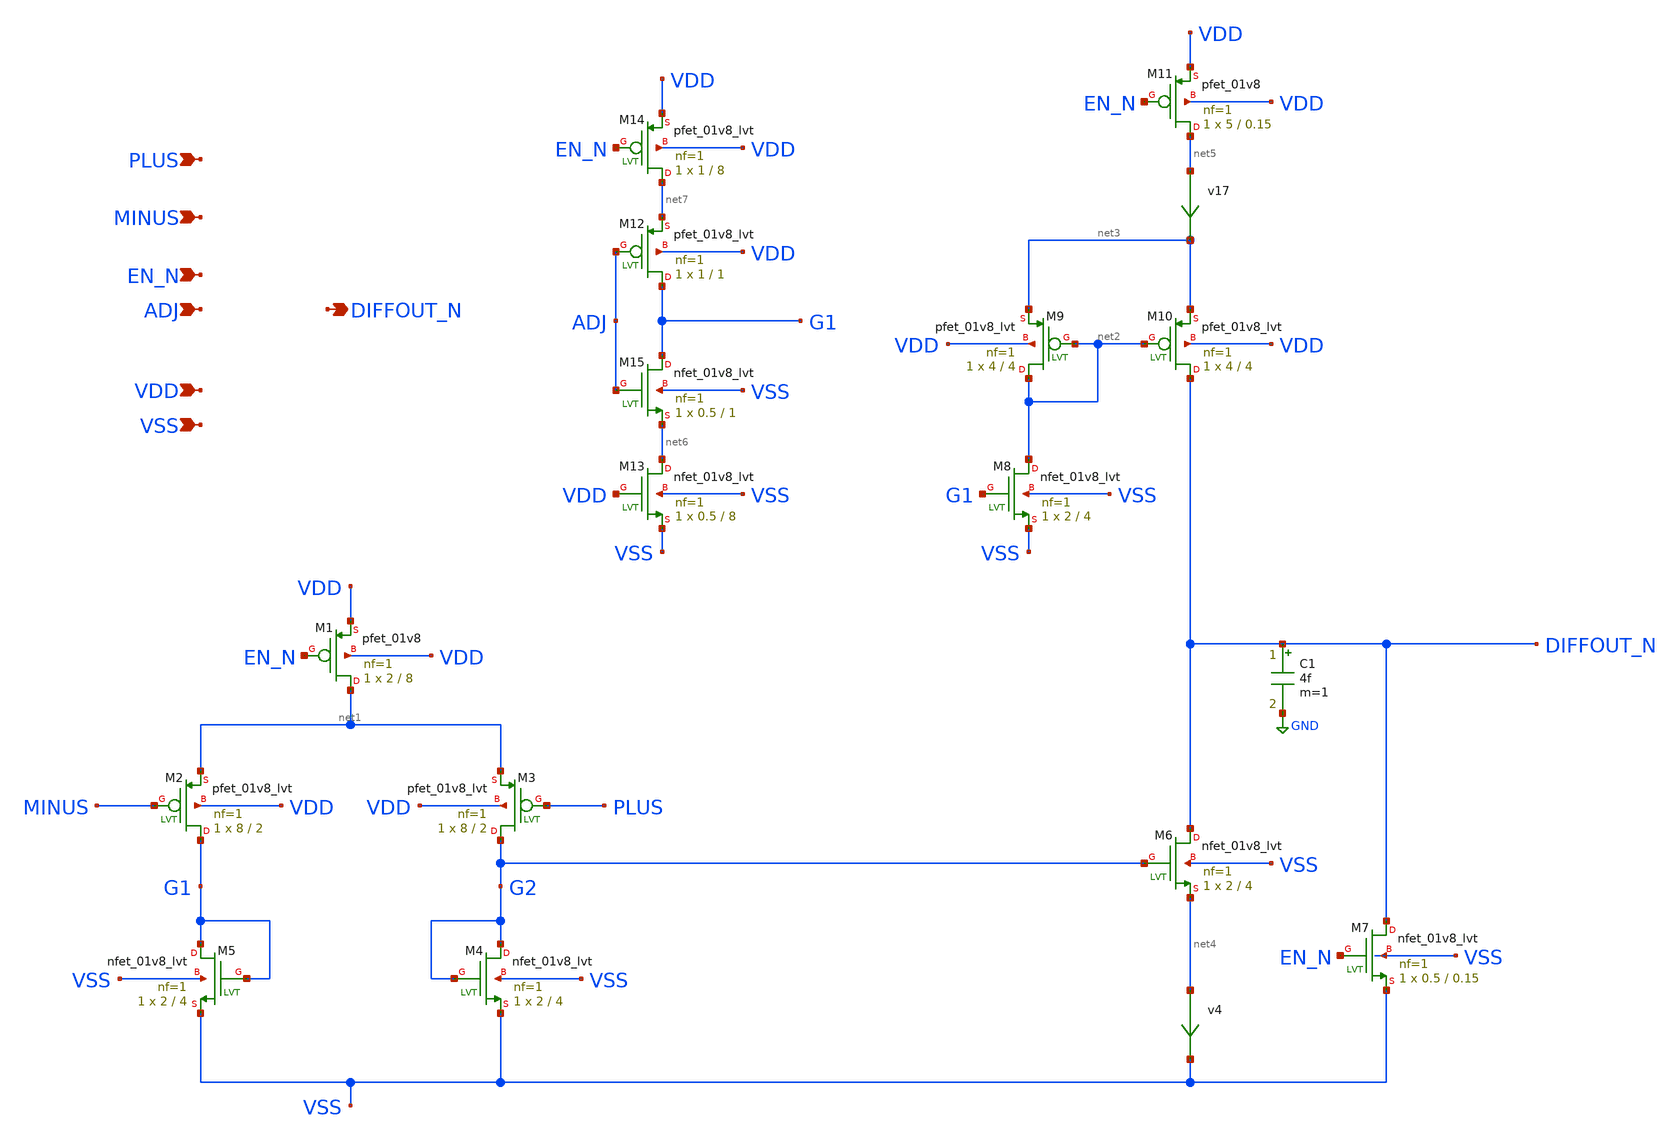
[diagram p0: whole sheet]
** sch_path: projects/pll/trials/opam.sch
**.subckt opam PLUS EN_N VDD VSS MINUS ADJ DIFFOUT_N
*.ipin PLUS
*.ipin EN_N
*.ipin VDD
*.ipin VSS
*.ipin MINUS
*.ipin ADJ
*.opin DIFFOUT_N
XM1 net1 EN_N VDD VDD sky130_fd_pr__pfet_01v8 L=8 W=2 nf=1 ad='int((nf+1)/2) * W/nf * 0.29' as='int((nf+2)/2) * W/nf * 0.29'
+ pd='2*int((nf+1)/2) * (W/nf + 0.29)' ps='2*int((nf+2)/2) * (W/nf + 0.29)' nrd='0.29 / W' nrs='0.29 / W'
+ sa=0 sb=0 sd=0 mult=1 m=1
XM2 G1 MINUS net1 VDD sky130_fd_pr__pfet_01v8_lvt L=2 W=8 nf=1 ad='int((nf+1)/2) * W/nf * 0.29' as='int((nf+2)/2) * W/nf * 0.29'
+ pd='2*int((nf+1)/2) * (W/nf + 0.29)' ps='2*int((nf+2)/2) * (W/nf + 0.29)' nrd='0.29 / W' nrs='0.29 / W'
+ sa=0 sb=0 sd=0 mult=1 m=1
XM3 G2 PLUS net1 VDD sky130_fd_pr__pfet_01v8_lvt L=2 W=8 nf=1 ad='int((nf+1)/2) * W/nf * 0.29' as='int((nf+2)/2) * W/nf * 0.29'
+ pd='2*int((nf+1)/2) * (W/nf + 0.29)' ps='2*int((nf+2)/2) * (W/nf + 0.29)' nrd='0.29 / W' nrs='0.29 / W'
+ sa=0 sb=0 sd=0 mult=1 m=1
XM4 G2 G2 VSS VSS sky130_fd_pr__nfet_01v8_lvt L=4 W=2 nf=1 ad='int((nf+1)/2) * W/nf * 0.29' as='int((nf+2)/2) * W/nf * 0.29'
+ pd='2*int((nf+1)/2) * (W/nf + 0.29)' ps='2*int((nf+2)/2) * (W/nf + 0.29)' nrd='0.29 / W' nrs='0.29 / W'
+ sa=0 sb=0 sd=0 mult=1 m=1
XM5 G1 G1 VSS VSS sky130_fd_pr__nfet_01v8_lvt L=4 W=2 nf=1 ad='int((nf+1)/2) * W/nf * 0.29' as='int((nf+2)/2) * W/nf * 0.29'
+ pd='2*int((nf+1)/2) * (W/nf + 0.29)' ps='2*int((nf+2)/2) * (W/nf + 0.29)' nrd='0.29 / W' nrs='0.29 / W'
+ sa=0 sb=0 sd=0 mult=1 m=1
XM6 DIFFOUT_N G2 net4 VSS sky130_fd_pr__nfet_01v8_lvt L=4 W=2 nf=1 ad='int((nf+1)/2) * W/nf * 0.29' as='int((nf+2)/2) * W/nf * 0.29'
+ pd='2*int((nf+1)/2) * (W/nf + 0.29)' ps='2*int((nf+2)/2) * (W/nf + 0.29)' nrd='0.29 / W' nrs='0.29 / W'
+ sa=0 sb=0 sd=0 mult=1 m=1
XM7 DIFFOUT_N EN_N VSS VSS sky130_fd_pr__nfet_01v8_lvt L=0.15 W=0.5 nf=1 ad='int((nf+1)/2) * W/nf * 0.29'
+ as='int((nf+2)/2) * W/nf * 0.29' pd='2*int((nf+1)/2) * (W/nf + 0.29)' ps='2*int((nf+2)/2) * (W/nf + 0.29)'
+ nrd='0.29 / W' nrs='0.29 / W' sa=0 sb=0 sd=0 mult=1 m=1
XM8 net2 G1 VSS VSS sky130_fd_pr__nfet_01v8_lvt L=4 W=2 nf=1 ad='int((nf+1)/2) * W/nf * 0.29' as='int((nf+2)/2) * W/nf * 0.29'
+ pd='2*int((nf+1)/2) * (W/nf + 0.29)' ps='2*int((nf+2)/2) * (W/nf + 0.29)' nrd='0.29 / W' nrs='0.29 / W'
+ sa=0 sb=0 sd=0 mult=1 m=1
XM9 net2 net2 net3 VDD sky130_fd_pr__pfet_01v8_lvt L=4 W=4 nf=1 ad='int((nf+1)/2) * W/nf * 0.29' as='int((nf+2)/2) * W/nf * 0.29'
+ pd='2*int((nf+1)/2) * (W/nf + 0.29)' ps='2*int((nf+2)/2) * (W/nf + 0.29)' nrd='0.29 / W' nrs='0.29 / W'
+ sa=0 sb=0 sd=0 mult=1 m=1
XM10 DIFFOUT_N net2 net3 VDD sky130_fd_pr__pfet_01v8_lvt L=4 W=4 nf=1 ad='int((nf+1)/2) * W/nf * 0.29'
+ as='int((nf+2)/2) * W/nf * 0.29' pd='2*int((nf+1)/2) * (W/nf + 0.29)' ps='2*int((nf+2)/2) * (W/nf + 0.29)'
+ nrd='0.29 / W' nrs='0.29 / W' sa=0 sb=0 sd=0 mult=1 m=1
v4 net4 VSS 0
.save i(v4)
v17 net5 net3 0
.save i(v17)
XM11 net5 EN_N VDD VDD sky130_fd_pr__pfet_01v8 L=0.15 W=5 nf=1 ad='int((nf+1)/2) * W/nf * 0.29' as='int((nf+2)/2) * W/nf * 0.29'
+ pd='2*int((nf+1)/2) * (W/nf + 0.29)' ps='2*int((nf+2)/2) * (W/nf + 0.29)' nrd='0.29 / W' nrs='0.29 / W'
+ sa=0 sb=0 sd=0 mult=1 m=1
C1 DIFFOUT_N GND 4f m=1
XM12 G1 ADJ net7 VDD sky130_fd_pr__pfet_01v8_lvt L=1 W=1 nf=1 ad='int((nf+1)/2) * W/nf * 0.29' as='int((nf+2)/2) * W/nf * 0.29'
+ pd='2*int((nf+1)/2) * (W/nf + 0.29)' ps='2*int((nf+2)/2) * (W/nf + 0.29)' nrd='0.29 / W' nrs='0.29 / W'
+ sa=0 sb=0 sd=0 mult=1 m=1
XM13 net6 VDD VSS VSS sky130_fd_pr__nfet_01v8_lvt L=8 W=0.5 nf=1 ad='int((nf+1)/2) * W/nf * 0.29' as='int((nf+2)/2) * W/nf * 0.29'
+ pd='2*int((nf+1)/2) * (W/nf + 0.29)' ps='2*int((nf+2)/2) * (W/nf + 0.29)' nrd='0.29 / W' nrs='0.29 / W'
+ sa=0 sb=0 sd=0 mult=1 m=1
XM14 net7 EN_N VDD VDD sky130_fd_pr__pfet_01v8_lvt L=8 W=1 nf=1 ad='int((nf+1)/2) * W/nf * 0.29' as='int((nf+2)/2) * W/nf * 0.29'
+ pd='2*int((nf+1)/2) * (W/nf + 0.29)' ps='2*int((nf+2)/2) * (W/nf + 0.29)' nrd='0.29 / W' nrs='0.29 / W'
+ sa=0 sb=0 sd=0 mult=1 m=1
XM15 G1 ADJ net6 VSS sky130_fd_pr__nfet_01v8_lvt L=1 W=0.5 nf=1 ad='int((nf+1)/2) * W/nf * 0.29' as='int((nf+2)/2) * W/nf * 0.29'
+ pd='2*int((nf+1)/2) * (W/nf + 0.29)' ps='2*int((nf+2)/2) * (W/nf + 0.29)' nrd='0.29 / W' nrs='0.29 / W'
+ sa=0 sb=0 sd=0 mult=1 m=1
**.ends
.GLOBAL GND
.end
